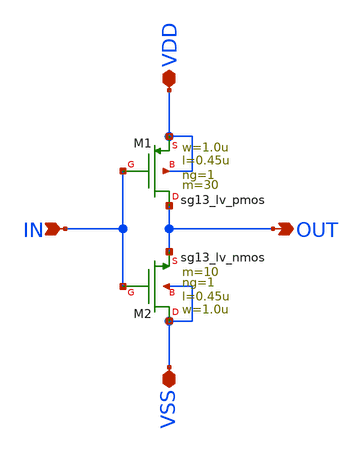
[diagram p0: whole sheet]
** sch_path: xschem/Ayudantias/Ayudantia_3/NMOS.sch
**.subckt NMOS VDD VSS OUT IN
*.iopin VDD
*.iopin VSS
*.opin OUT
*.ipin IN
XM1 OUT IN VDD VDD sg13_lv_pmos w=1.0u l=0.45u ng=1 m=30 mm_ok=1
XM2 VSS IN OUT VSS sg13_lv_nmos w=1.0u l=0.45u ng=1 m=10 mm_ok=1
**.ends
.end
